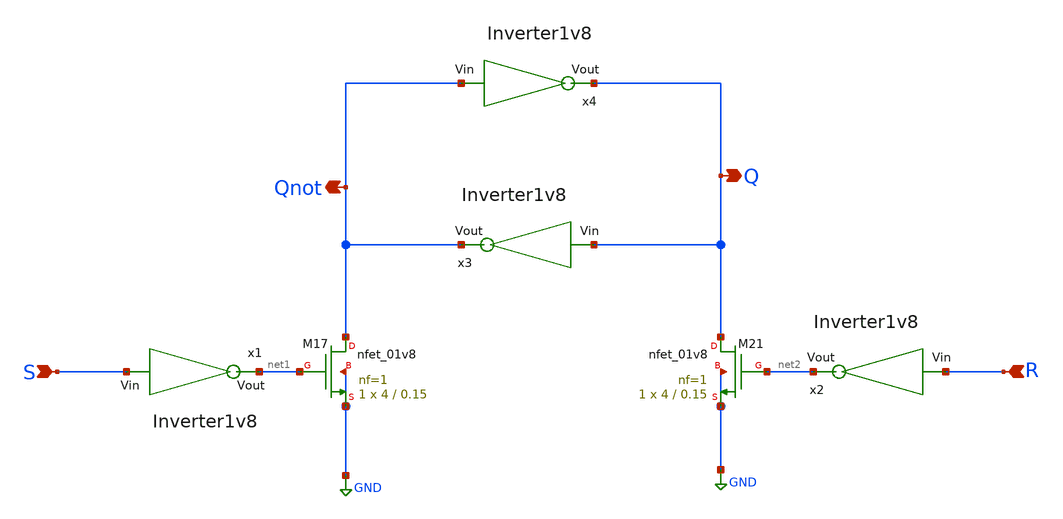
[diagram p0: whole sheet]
** sch_path: xschem/StandardCells/SRlatch.sch
**.subckt SRlatch S R Qnot Q
*.ipin S
*.ipin R
*.opin Qnot
*.opin Q
x1 S net1 Inverter1v8
XM17 Qnot net1 GND GND sky130_fd_pr__nfet_01v8 L=0.15 W=4 nf=1 ad='int((nf+1)/2) * W/nf * 0.29' as='int((nf+2)/2) * W/nf * 0.29'
+ pd='2*int((nf+1)/2) * (W/nf + 0.29)' ps='2*int((nf+2)/2) * (W/nf + 0.29)' nrd='0.29 / W' nrs='0.29 / W'
+ sa=0 sb=0 sd=0 mult=1 m=1
x2 R net2 Inverter1v8
XM21 Q net2 GND GND sky130_fd_pr__nfet_01v8 L=0.15 W=4 nf=1 ad='int((nf+1)/2) * W/nf * 0.29' as='int((nf+2)/2) * W/nf * 0.29'
+ pd='2*int((nf+1)/2) * (W/nf + 0.29)' ps='2*int((nf+2)/2) * (W/nf + 0.29)' nrd='0.29 / W' nrs='0.29 / W'
+ sa=0 sb=0 sd=0 mult=1 m=1
x3 Q Qnot Inverter1v8
x4 Qnot Q Inverter1v8
**.ends
.GLOBAL GND
.end
